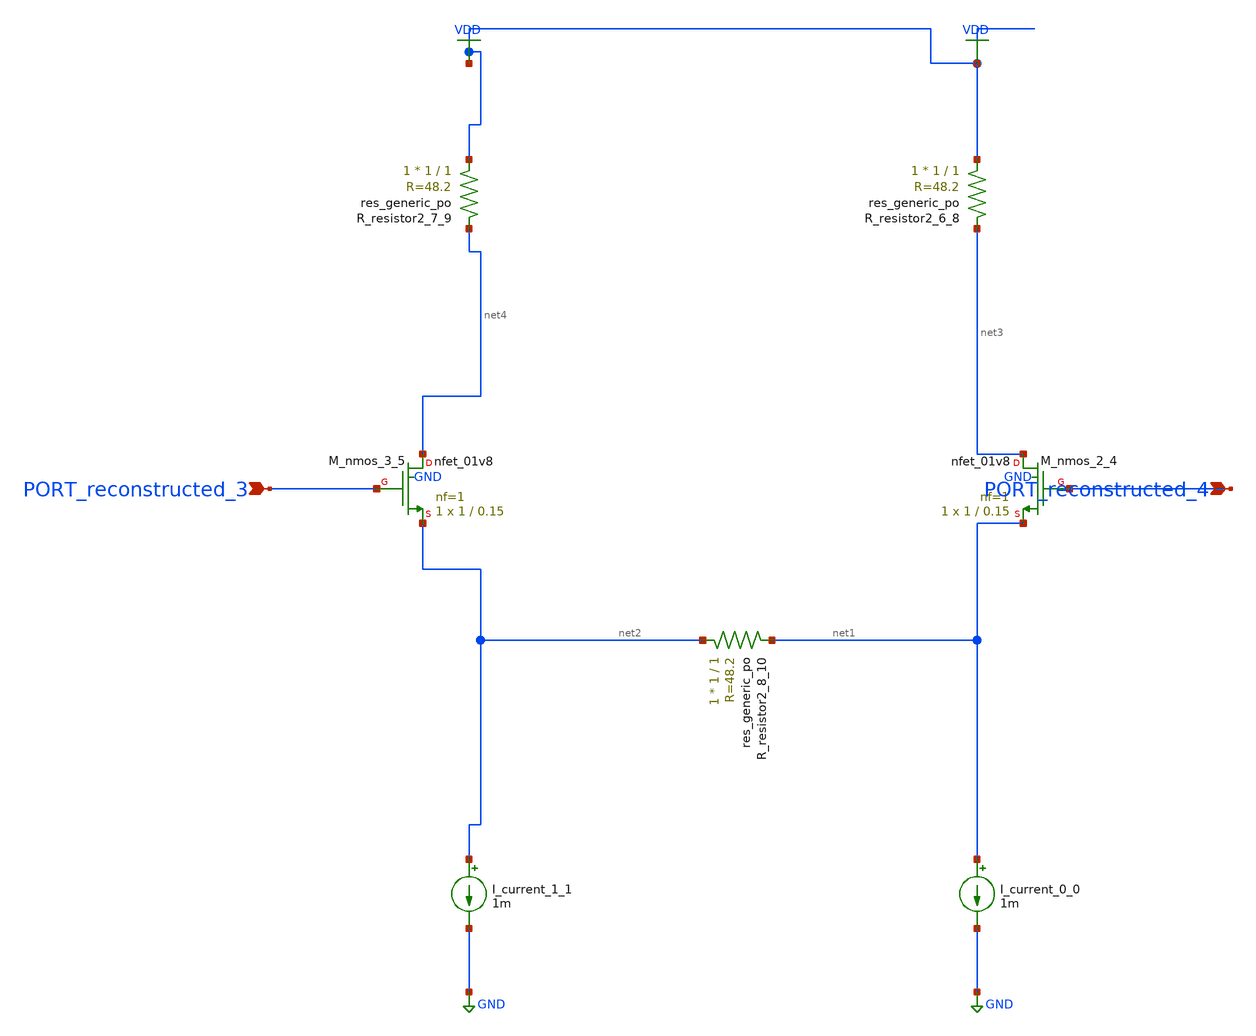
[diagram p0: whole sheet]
** sch_path: schematics/AMSNet/209.sch
**.subckt 209 PORT_reconstructed_3 PORT_reconstructed_4
*.ipin PORT_reconstructed_3
*.ipin PORT_reconstructed_4
I_current_0_0 net1 GND 1m
I_current_1_1 net2 GND 1m
XM_nmos_2_4 net3 PORT_reconstructed_4 net1 GND sky130_fd_pr__nfet_01v8 L=0.15 W=1 nf=1 ad='int((1 + 1)/2) * 1 / 1 * 0.29'
+ as='int((1 + 2)/2) * 1 / 1 * 0.29' pd='2*int((1 + 1)/2) * (1 / 1 + 0.29)' ps='2*int((1 + 2)/2) * (1 / 1 + 0.29)'
+ nrd='0.29 / 1 ' nrs='0.29 / 1 ' sa=0 sb=0 sd=0 mult=1 m=1
XM_nmos_3_5 net4 PORT_reconstructed_3 net2 GND sky130_fd_pr__nfet_01v8 L=0.15 W=1 nf=1 ad='int((1 + 1)/2) * 1 / 1 * 0.29'
+ as='int((1 + 2)/2) * 1 / 1 * 0.29' pd='2*int((1 + 1)/2) * (1 / 1 + 0.29)' ps='2*int((1 + 2)/2) * (1 / 1 + 0.29)'
+ nrd='0.29 / 1 ' nrs='0.29 / 1 ' sa=0 sb=0 sd=0 mult=1 m=1
XR_resistor2_6_8 VDD net3 sky130_fd_pr__res_generic_po W=1 L=1 m=1
XR_resistor2_7_9 VDD net4 sky130_fd_pr__res_generic_po W=1 L=1 m=1
XR_resistor2_8_10 net2 net1 sky130_fd_pr__res_generic_po W=1 L=1 m=1
**.ends
.GLOBAL GND
.GLOBAL VDD
.end
